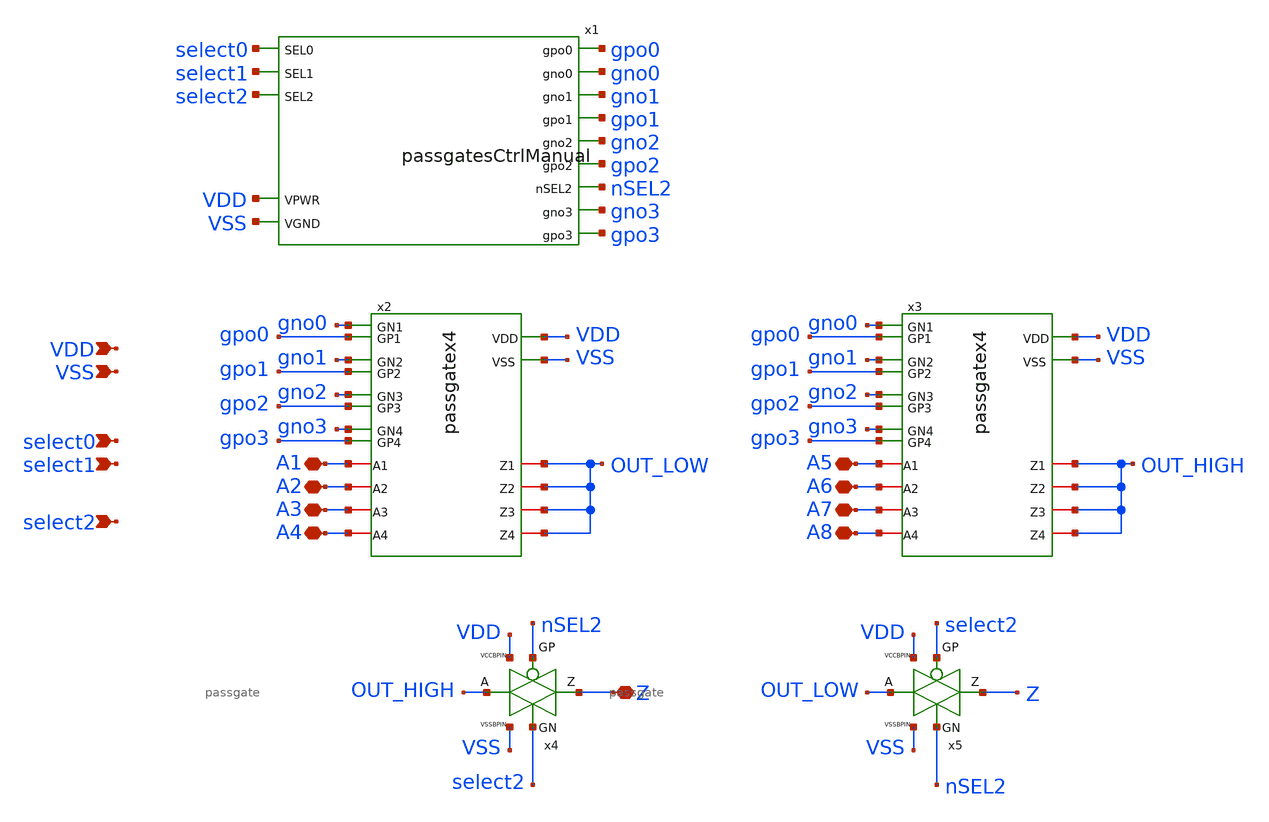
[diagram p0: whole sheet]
** sch_path: xschem/mux8onehot.sch
**.subckt mux8onehot select0 select1 select2 VDD VSS Z A1 A2 A3 A4 A5 A6 A7 A8
*.ipin select0
*.ipin select1
*.ipin select2
*.ipin VDD
*.ipin VSS
*.iopin Z
*.iopin A1
*.iopin A2
*.iopin A3
*.iopin A4
*.iopin A5
*.iopin A6
*.iopin A7
*.iopin A8
x4 Z OUT_HIGH nSEL2 select2 VSS VDD passgate
x5 Z OUT_LOW select2 nSEL2 VSS VDD passgate
x2 gpo2 gpo1 gpo0 VDD gpo3 VSS A3 A2 A1 OUT_LOW OUT_LOW OUT_LOW A4 OUT_LOW gno2 gno1 gno0 gno3
+ passgatex4
x1 gpo0 gno0 gno1 gpo1 select0 select1 gno2 gpo2 nSEL2 select2 gno3 gpo3 VDD VSS passgatesCtrlManual
x3 gpo2 gpo1 gpo0 VDD gpo3 VSS A7 A6 A5 OUT_HIGH OUT_HIGH OUT_HIGH A8 OUT_HIGH gno2 gno1 gno0 gno3
+ passgatex4
**.ends
.end
